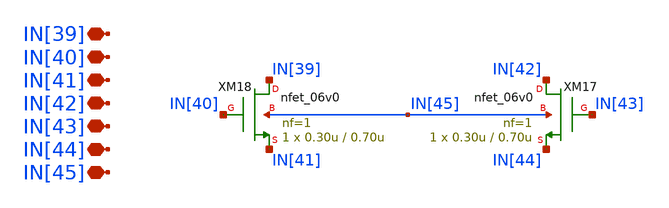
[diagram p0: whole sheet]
** sch_path: designs/libs/core_single-fet/nfet-pin/nfet-pin.sch
**.subckt nfet-pin IN[39] IN[40] IN[41] IN[42] IN[43] IN[44] IN[45]
*.iopin IN[39]
*.iopin IN[40]
*.iopin IN[41]
*.iopin IN[42]
*.iopin IN[43]
*.iopin IN[44]
*.iopin IN[45]
XM17 IN[42] IN[43] IN[44] IN[45] nfet_06v0 L=0.70u W=0.30u nf=1 ad='int((nf+1)/2) * W/nf * 0.18u' as='int((nf+2)/2) * W/nf * 0.18u'
+ pd='2*int((nf+1)/2) * (W/nf + 0.18u)' ps='2*int((nf+2)/2) * (W/nf + 0.18u)' nrd='0.18u / W' nrs='0.18u / W'
+ sa=0 sb=0 sd=0 m=1
XM18 IN[39] IN[40] IN[41] IN[45] nfet_06v0 L=0.70u W=0.30u nf=1 ad='int((nf+1)/2) * W/nf * 0.18u' as='int((nf+2)/2) * W/nf * 0.18u'
+ pd='2*int((nf+1)/2) * (W/nf + 0.18u)' ps='2*int((nf+2)/2) * (W/nf + 0.18u)' nrd='0.18u / W' nrs='0.18u / W'
+ sa=0 sb=0 sd=0 m=1
**.ends
.end
